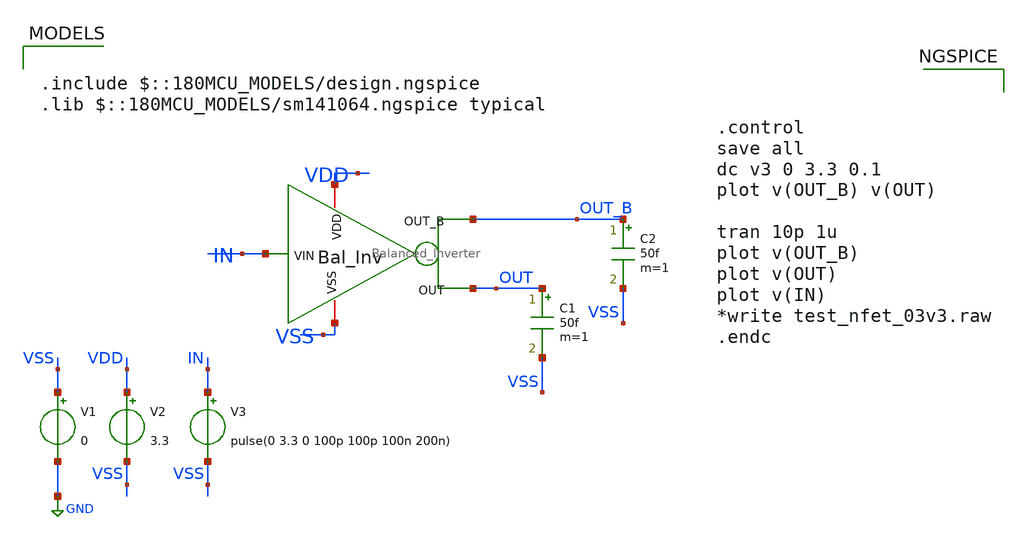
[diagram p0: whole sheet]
** sch_path: DAC_PAKISTAN_01/Pakistan1_Xschem/BAL_INV_TB.sch
**.subckt BAL_INV_TB
x1 VDD VSS IN OUT_B OUT Balanced_Inverter
V1 VSS GND 0
V2 VDD VSS 3.3
V3 IN VSS pulse(0 3.3 0 100p 100p 100n 200n)
C1 OUT VSS 50f m=1
C2 OUT_B VSS 50f m=1
**** begin user architecture code

.include $::180MCU_MODELS/design.ngspice
.lib $::180MCU_MODELS/sm141064.ngspice typical




.control
save all
dc v3 0 3.3 0.1
plot v(OUT_B) v(OUT)

tran 10p 1u
plot v(OUT_B)
plot v(OUT)
plot v(IN)
*write test_nfet_03v3.raw
.endc


**** end user architecture code
**.ends

* expanding   symbol:  Balanced_Inverter.sym # of pins=5
** sym_path: DAC_PAKISTAN_01/Pakistan1_Xschem/Balanced_Inverter.sym
** sch_path: DAC_PAKISTAN_01/Pakistan1_Xschem/Balanced_Inverter.sch
.subckt Balanced_Inverter VDD VSS VIN OUT_B OUT
*.iopin VSS
*.ipin VIN
*.opin OUT_B
*.iopin VDD
*.opin OUT
XM1 OUT_B VIN VSS VSS nfet_03v3 L=0.28u W=0.22u nf=1 ad='int((nf+1)/2) * W/nf * 0.18u' as='int((nf+2)/2) * W/nf * 0.18u'
+ pd='2*int((nf+1)/2) * (W/nf + 0.18u)' ps='2*int((nf+2)/2) * (W/nf + 0.18u)' nrd='0.18u / W' nrs='0.18u / W'
+ sa=0 sb=0 sd=0 m=1
XM2 OUT_B OUT VDD VDD pfet_03v3 L=0.28u W=0.22u nf=1 ad='int((nf+1)/2) * W/nf * 0.18u' as='int((nf+2)/2) * W/nf * 0.18u'
+ pd='2*int((nf+1)/2) * (W/nf + 0.18u)' ps='2*int((nf+2)/2) * (W/nf + 0.18u)' nrd='0.18u / W' nrs='0.18u / W'
+ sa=0 sb=0 sd=0 m=1
XM3 OUT net1 VSS VSS nfet_03v3 L=0.28u W=0.22u nf=1 ad='int((nf+1)/2) * W/nf * 0.18u' as='int((nf+2)/2) * W/nf * 0.18u'
+ pd='2*int((nf+1)/2) * (W/nf + 0.18u)' ps='2*int((nf+2)/2) * (W/nf + 0.18u)' nrd='0.18u / W' nrs='0.18u / W'
+ sa=0 sb=0 sd=0 m=1
XM4 OUT OUT_B VDD VDD pfet_03v3 L=0.28u W=0.22u nf=1 ad='int((nf+1)/2) * W/nf * 0.18u' as='int((nf+2)/2) * W/nf * 0.18u'
+ pd='2*int((nf+1)/2) * (W/nf + 0.18u)' ps='2*int((nf+2)/2) * (W/nf + 0.18u)' nrd='0.18u / W' nrs='0.18u / W'
+ sa=0 sb=0 sd=0 m=1
x1 VSS VDD net1 VIN GF_INV
.ends


* expanding   symbol:  GF_INV.sym # of pins=4
** sym_path: GF_INV.sym
** sch_path: GF_INV.sch
.subckt GF_INV VSS VDD OUT IN
*.iopin VDD
*.iopin VSS
*.ipin IN
*.opin OUT
XM1 OUT IN VSS VSS nfet_03v3 L=0.28u W=0.25u nf=1 ad='int((nf+1)/2) * W/nf * 0.18u' as='int((nf+2)/2) * W/nf * 0.18u'
+ pd='2*int((nf+1)/2) * (W/nf + 0.18u)' ps='2*int((nf+2)/2) * (W/nf + 0.18u)' nrd='0.18u / W' nrs='0.18u / W'
+ sa=0 sb=0 sd=0 m=1
XM2 OUT IN VDD VDD pfet_03v3 L=0.28u W=0.5u nf=1 ad='int((nf+1)/2) * W/nf * 0.18u' as='int((nf+2)/2) * W/nf * 0.18u'
+ pd='2*int((nf+1)/2) * (W/nf + 0.18u)' ps='2*int((nf+2)/2) * (W/nf + 0.18u)' nrd='0.18u / W' nrs='0.18u / W'
+ sa=0 sb=0 sd=0 m=1
.ends

.GLOBAL GND
.end
